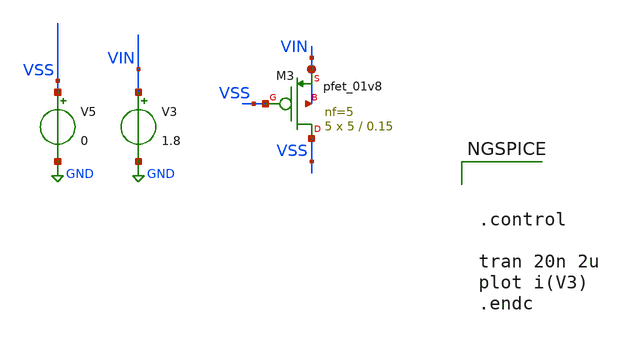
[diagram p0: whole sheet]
** sch_path: xschem/DC_DC_Converter_xschem/OTHERS/TWF_test.sch
**.subckt TWF_test
XM3 VSS VSS VIN VIN sky130_fd_pr__pfet_01v8 L=0.15 W=5 nf=5 ad='int((nf+1)/2) * W/nf * 0.29' as='int((nf+2)/2) * W/nf * 0.29'
+ pd='2*int((nf+1)/2) * (W/nf + 0.29)' ps='2*int((nf+2)/2) * (W/nf + 0.29)' nrd='0.29 / W' nrs='0.29 / W'
+ sa=0 sb=0 sd=0 mult=5 m=5
V3 VIN GND 1.8
V5 VSS GND 0
**** begin user architecture code



.control

tran 20n 2u
plot i(V3)
.endc


** manual skywater pdks install (with patches applied)
* .lib $::SKYWATER_MODELS/models/sky130.lib.spice tt

** opencircuitdesign pdks install
.lib $::SKYWATER_MODELS/sky130.lib.spice tt
.include $::SKYWATER_STDCELLS/sky130_fd_sc_hd.spice

**** end user architecture code
**.ends
.GLOBAL GND
.end
